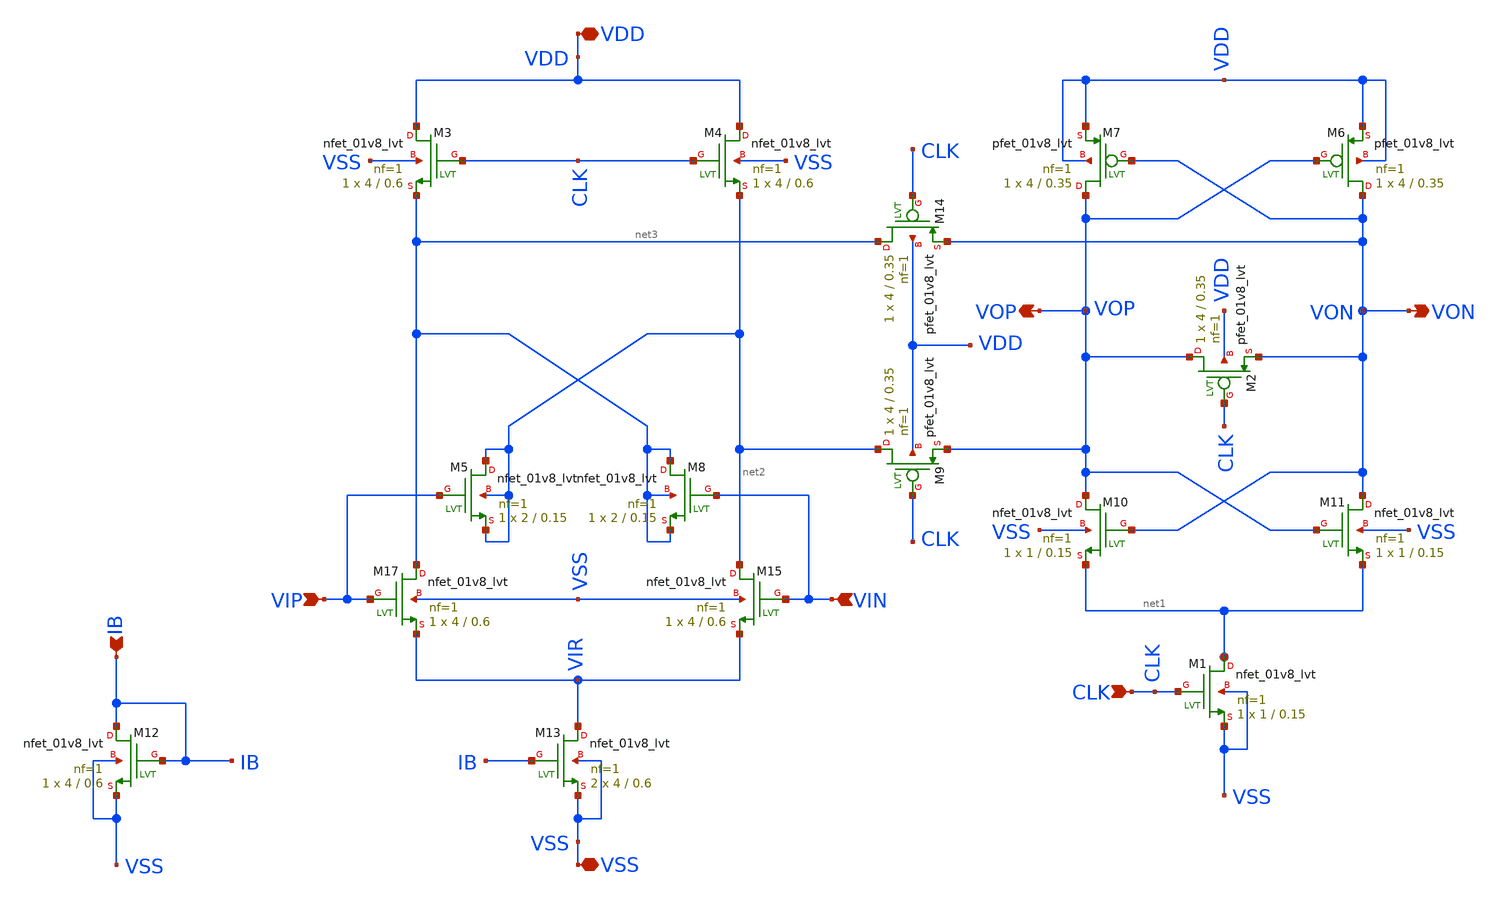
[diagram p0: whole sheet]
** sch_path: flashADC/xschem/class_AB_v2_sym.sch
**.subckt class_AB_v2_sym VDD IB VSS VIP VIN VON VOP CLK
*.iopin VDD
*.ipin IB
*.iopin VSS
*.ipin VIP
*.ipin VIN
*.opin VON
*.opin VOP
*.ipin CLK
XM17 net3 VIP VIR VSS sky130_fd_pr__nfet_01v8_lvt L=0.6 W=4 nf=1 ad='int((nf+1)/2) * W/nf * 0.29' as='int((nf+2)/2) * W/nf * 0.29'
+ pd='2*int((nf+1)/2) * (W/nf + 0.29)' ps='2*int((nf+2)/2) * (W/nf + 0.29)' nrd='0.29 / W' nrs='0.29 / W'
+ sa=0 sb=0 sd=0 mult=1 m=1
XM12 IB IB VSS VSS sky130_fd_pr__nfet_01v8_lvt L=0.6 W=4 nf=1 ad='int((nf+1)/2) * W/nf * 0.29' as='int((nf+2)/2) * W/nf * 0.29'
+ pd='2*int((nf+1)/2) * (W/nf + 0.29)' ps='2*int((nf+2)/2) * (W/nf + 0.29)' nrd='0.29 / W' nrs='0.29 / W'
+ sa=0 sb=0 sd=0 mult=1 m=1
XM15 net2 VIN VIR VSS sky130_fd_pr__nfet_01v8_lvt L=0.6 W=4 nf=1 ad='int((nf+1)/2) * W/nf * 0.29' as='int((nf+2)/2) * W/nf * 0.29'
+ pd='2*int((nf+1)/2) * (W/nf + 0.29)' ps='2*int((nf+2)/2) * (W/nf + 0.29)' nrd='0.29 / W' nrs='0.29 / W'
+ sa=0 sb=0 sd=0 mult=1 m=1
XM13 VIR IB VSS VSS sky130_fd_pr__nfet_01v8_lvt L=0.6 W=4 nf=1 ad='int((nf+1)/2) * W/nf * 0.29' as='int((nf+2)/2) * W/nf * 0.29'
+ pd='2*int((nf+1)/2) * (W/nf + 0.29)' ps='2*int((nf+2)/2) * (W/nf + 0.29)' nrd='0.29 / W' nrs='0.29 / W'
+ sa=0 sb=0 sd=0 mult=2 m=2
XM6 VON VOP VDD VDD sky130_fd_pr__pfet_01v8_lvt L=0.35 W=4 nf=1 ad='int((nf+1)/2) * W/nf * 0.29' as='int((nf+2)/2) * W/nf * 0.29'
+ pd='2*int((nf+1)/2) * (W/nf + 0.29)' ps='2*int((nf+2)/2) * (W/nf + 0.29)' nrd='0.29 / W' nrs='0.29 / W'
+ sa=0 sb=0 sd=0 mult=1 m=1
XM7 VOP VON VDD VDD sky130_fd_pr__pfet_01v8_lvt L=0.35 W=4 nf=1 ad='int((nf+1)/2) * W/nf * 0.29' as='int((nf+2)/2) * W/nf * 0.29'
+ pd='2*int((nf+1)/2) * (W/nf + 0.29)' ps='2*int((nf+2)/2) * (W/nf + 0.29)' nrd='0.29 / W' nrs='0.29 / W'
+ sa=0 sb=0 sd=0 mult=1 m=1
XM10 VOP VON net1 VSS sky130_fd_pr__nfet_01v8_lvt L=0.15 W=1 nf=1 ad='int((nf+1)/2) * W/nf * 0.29' as='int((nf+2)/2) * W/nf * 0.29'
+ pd='2*int((nf+1)/2) * (W/nf + 0.29)' ps='2*int((nf+2)/2) * (W/nf + 0.29)' nrd='0.29 / W' nrs='0.29 / W'
+ sa=0 sb=0 sd=0 mult=1 m=1
XM11 VON VOP net1 VSS sky130_fd_pr__nfet_01v8_lvt L=0.15 W=1 nf=1 ad='int((nf+1)/2) * W/nf * 0.29' as='int((nf+2)/2) * W/nf * 0.29'
+ pd='2*int((nf+1)/2) * (W/nf + 0.29)' ps='2*int((nf+2)/2) * (W/nf + 0.29)' nrd='0.29 / W' nrs='0.29 / W'
+ sa=0 sb=0 sd=0 mult=1 m=1
XM1 net1 CLK VSS VSS sky130_fd_pr__nfet_01v8_lvt L=0.15 W=1 nf=1 ad='int((nf+1)/2) * W/nf * 0.29' as='int((nf+2)/2) * W/nf * 0.29'
+ pd='2*int((nf+1)/2) * (W/nf + 0.29)' ps='2*int((nf+2)/2) * (W/nf + 0.29)' nrd='0.29 / W' nrs='0.29 / W'
+ sa=0 sb=0 sd=0 mult=1 m=1
XM2 VOP CLK VON VDD sky130_fd_pr__pfet_01v8_lvt L=0.35 W=4 nf=1 ad='int((nf+1)/2) * W/nf * 0.29' as='int((nf+2)/2) * W/nf * 0.29'
+ pd='2*int((nf+1)/2) * (W/nf + 0.29)' ps='2*int((nf+2)/2) * (W/nf + 0.29)' nrd='0.29 / W' nrs='0.29 / W'
+ sa=0 sb=0 sd=0 mult=1 m=1
XM5 net2 VIP net2 net2 sky130_fd_pr__nfet_01v8_lvt L=0.15 W=2 nf=1 ad='int((nf+1)/2) * W/nf * 0.29' as='int((nf+2)/2) * W/nf * 0.29'
+ pd='2*int((nf+1)/2) * (W/nf + 0.29)' ps='2*int((nf+2)/2) * (W/nf + 0.29)' nrd='0.29 / W' nrs='0.29 / W'
+ sa=0 sb=0 sd=0 mult=1 m=1
XM8 net3 VIN net3 net3 sky130_fd_pr__nfet_01v8_lvt L=0.15 W=2 nf=1 ad='int((nf+1)/2) * W/nf * 0.29' as='int((nf+2)/2) * W/nf * 0.29'
+ pd='2*int((nf+1)/2) * (W/nf + 0.29)' ps='2*int((nf+2)/2) * (W/nf + 0.29)' nrd='0.29 / W' nrs='0.29 / W'
+ sa=0 sb=0 sd=0 mult=1 m=1
XM9 net2 CLK VOP VDD sky130_fd_pr__pfet_01v8_lvt L=0.35 W=4 nf=1 ad='int((nf+1)/2) * W/nf * 0.29' as='int((nf+2)/2) * W/nf * 0.29'
+ pd='2*int((nf+1)/2) * (W/nf + 0.29)' ps='2*int((nf+2)/2) * (W/nf + 0.29)' nrd='0.29 / W' nrs='0.29 / W'
+ sa=0 sb=0 sd=0 mult=1 m=1
XM14 net3 CLK VON VDD sky130_fd_pr__pfet_01v8_lvt L=0.35 W=4 nf=1 ad='int((nf+1)/2) * W/nf * 0.29' as='int((nf+2)/2) * W/nf * 0.29'
+ pd='2*int((nf+1)/2) * (W/nf + 0.29)' ps='2*int((nf+2)/2) * (W/nf + 0.29)' nrd='0.29 / W' nrs='0.29 / W'
+ sa=0 sb=0 sd=0 mult=1 m=1
XM3 VDD CLK net3 VSS sky130_fd_pr__nfet_01v8_lvt L=0.6 W=4 nf=1 ad='int((nf+1)/2) * W/nf * 0.29' as='int((nf+2)/2) * W/nf * 0.29'
+ pd='2*int((nf+1)/2) * (W/nf + 0.29)' ps='2*int((nf+2)/2) * (W/nf + 0.29)' nrd='0.29 / W' nrs='0.29 / W'
+ sa=0 sb=0 sd=0 mult=1 m=1
XM4 VDD CLK net2 VSS sky130_fd_pr__nfet_01v8_lvt L=0.6 W=4 nf=1 ad='int((nf+1)/2) * W/nf * 0.29' as='int((nf+2)/2) * W/nf * 0.29'
+ pd='2*int((nf+1)/2) * (W/nf + 0.29)' ps='2*int((nf+2)/2) * (W/nf + 0.29)' nrd='0.29 / W' nrs='0.29 / W'
+ sa=0 sb=0 sd=0 mult=1 m=1
**.ends
.end
